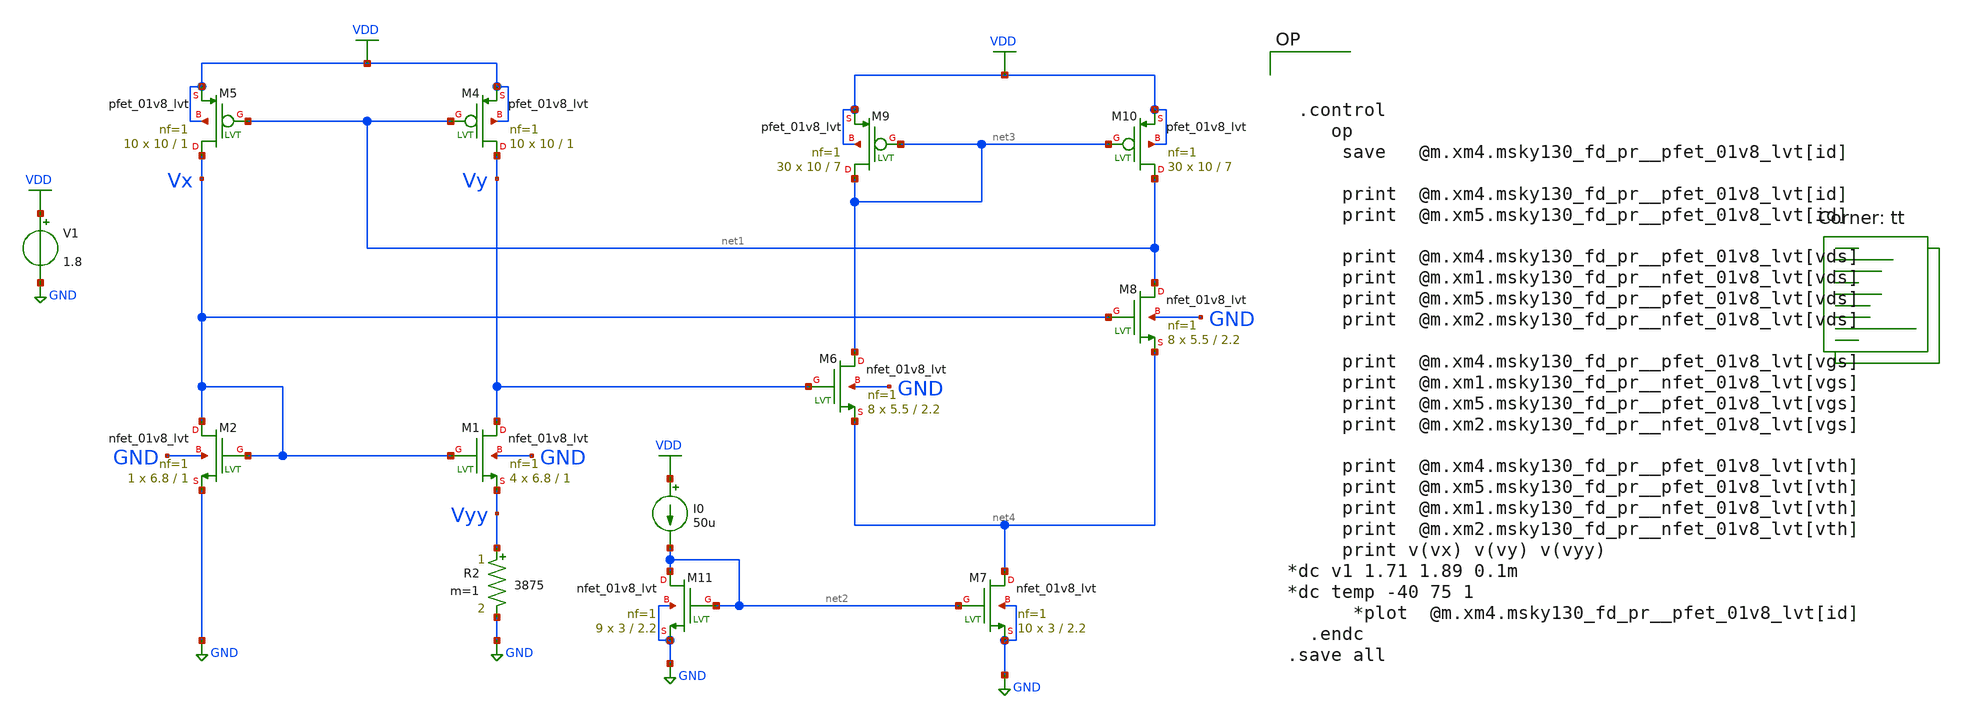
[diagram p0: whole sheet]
** sch_path: pll/lc_vco_lib/Hossam_Tarek/Biasing Circuits/xschem/constant GM2 1.sch
**.subckt constant GM2 1
XM1 Vy Vx Vyy GND sky130_fd_pr__nfet_01v8_lvt L=1 W=6.8 nf=1 ad='int((nf+1)/2) * W/nf * 0.29' as='int((nf+2)/2) * W/nf * 0.29'
+ pd='2*int((nf+1)/2) * (W/nf + 0.29)' ps='2*int((nf+2)/2) * (W/nf + 0.29)' nrd='0.29 / W' nrs='0.29 / W'
+ sa=0 sb=0 sd=0 mult=4 m=4
XM2 Vx Vx GND GND sky130_fd_pr__nfet_01v8_lvt L=1 W=6.8 nf=1 ad='int((nf+1)/2) * W/nf * 0.29' as='int((nf+2)/2) * W/nf * 0.29'
+ pd='2*int((nf+1)/2) * (W/nf + 0.29)' ps='2*int((nf+2)/2) * (W/nf + 0.29)' nrd='0.29 / W' nrs='0.29 / W'
+ sa=0 sb=0 sd=0 mult=1 m=1
XM4 Vy net1 VDD VDD sky130_fd_pr__pfet_01v8_lvt L=1 W=10 nf=1 ad='int((nf+1)/2) * W/nf * 0.29' as='int((nf+2)/2) * W/nf * 0.29'
+ pd='2*int((nf+1)/2) * (W/nf + 0.29)' ps='2*int((nf+2)/2) * (W/nf + 0.29)' nrd='0.29 / W' nrs='0.29 / W'
+ sa=0 sb=0 sd=0 mult=10 m=10
XM5 Vx net1 VDD VDD sky130_fd_pr__pfet_01v8_lvt L=1 W=10 nf=1 ad='int((nf+1)/2) * W/nf * 0.29' as='int((nf+2)/2) * W/nf * 0.29'
+ pd='2*int((nf+1)/2) * (W/nf + 0.29)' ps='2*int((nf+2)/2) * (W/nf + 0.29)' nrd='0.29 / W' nrs='0.29 / W'
+ sa=0 sb=0 sd=0 mult=10 m=10
R2 Vyy GND 3875 m=1
V1 VDD GND 1.8
XM6 net3 Vy net4 GND sky130_fd_pr__nfet_01v8_lvt L=2.2 W=5.5 nf=1 ad='int((nf+1)/2) * W/nf * 0.29' as='int((nf+2)/2) * W/nf * 0.29'
+ pd='2*int((nf+1)/2) * (W/nf + 0.29)' ps='2*int((nf+2)/2) * (W/nf + 0.29)' nrd='0.29 / W' nrs='0.29 / W'
+ sa=0 sb=0 sd=0 mult=8 m=8
XM7 net4 net2 GND GND sky130_fd_pr__nfet_01v8_lvt L=2.2 W=3 nf=1 ad='int((nf+1)/2) * W/nf * 0.29' as='int((nf+2)/2) * W/nf * 0.29'
+ pd='2*int((nf+1)/2) * (W/nf + 0.29)' ps='2*int((nf+2)/2) * (W/nf + 0.29)' nrd='0.29 / W' nrs='0.29 / W'
+ sa=0 sb=0 sd=0 mult=10 m=10
XM8 net1 Vx net4 GND sky130_fd_pr__nfet_01v8_lvt L=2.2 W=5.5 nf=1 ad='int((nf+1)/2) * W/nf * 0.29' as='int((nf+2)/2) * W/nf * 0.29'
+ pd='2*int((nf+1)/2) * (W/nf + 0.29)' ps='2*int((nf+2)/2) * (W/nf + 0.29)' nrd='0.29 / W' nrs='0.29 / W'
+ sa=0 sb=0 sd=0 mult=8 m=8
XM9 net3 net3 VDD VDD sky130_fd_pr__pfet_01v8_lvt L=7 W=10 nf=1 ad='int((nf+1)/2) * W/nf * 0.29' as='int((nf+2)/2) * W/nf * 0.29'
+ pd='2*int((nf+1)/2) * (W/nf + 0.29)' ps='2*int((nf+2)/2) * (W/nf + 0.29)' nrd='0.29 / W' nrs='0.29 / W'
+ sa=0 sb=0 sd=0 mult=30 m=30
XM10 net1 net3 VDD VDD sky130_fd_pr__pfet_01v8_lvt L=7 W=10 nf=1 ad='int((nf+1)/2) * W/nf * 0.29' as='int((nf+2)/2) * W/nf * 0.29'
+ pd='2*int((nf+1)/2) * (W/nf + 0.29)' ps='2*int((nf+2)/2) * (W/nf + 0.29)' nrd='0.29 / W' nrs='0.29 / W'
+ sa=0 sb=0 sd=0 mult=30 m=30
XM11 net2 net2 GND GND sky130_fd_pr__nfet_01v8_lvt L=2.2 W=3 nf=1 ad='int((nf+1)/2) * W/nf * 0.29' as='int((nf+2)/2) * W/nf * 0.29'
+ pd='2*int((nf+1)/2) * (W/nf + 0.29)' ps='2*int((nf+2)/2) * (W/nf + 0.29)' nrd='0.29 / W' nrs='0.29 / W'
+ sa=0 sb=0 sd=0 mult=9 m=9
I0 VDD net2 50u
**** begin user architecture code



 .control
    op
     save   @m.xm4.msky130_fd_pr__pfet_01v8_lvt[id]

     print  @m.xm4.msky130_fd_pr__pfet_01v8_lvt[id]
     print  @m.xm5.msky130_fd_pr__pfet_01v8_lvt[id]

     print  @m.xm4.msky130_fd_pr__pfet_01v8_lvt[vds]
     print  @m.xm1.msky130_fd_pr__nfet_01v8_lvt[vds]
     print  @m.xm5.msky130_fd_pr__pfet_01v8_lvt[vds]
     print  @m.xm2.msky130_fd_pr__nfet_01v8_lvt[vds]

     print  @m.xm4.msky130_fd_pr__pfet_01v8_lvt[vgs]
     print  @m.xm1.msky130_fd_pr__nfet_01v8_lvt[vgs]
     print  @m.xm5.msky130_fd_pr__pfet_01v8_lvt[vgs]
     print  @m.xm2.msky130_fd_pr__nfet_01v8_lvt[vgs]

     print  @m.xm4.msky130_fd_pr__pfet_01v8_lvt[vth]
     print  @m.xm5.msky130_fd_pr__pfet_01v8_lvt[vth]
     print  @m.xm1.msky130_fd_pr__nfet_01v8_lvt[vth]
     print  @m.xm2.msky130_fd_pr__nfet_01v8_lvt[vth]
     print v(vx) v(vy) v(vyy)
*dc v1 1.71 1.89 0.1m
*dc temp -40 75 1
      *plot  @m.xm4.msky130_fd_pr__pfet_01v8_lvt[id]
  .endc
.save all

.lib $::SKYWATER_MODELS/sky130.lib.spice tt
**** end user architecture code
**.ends
.GLOBAL GND
.GLOBAL VDD
.end
